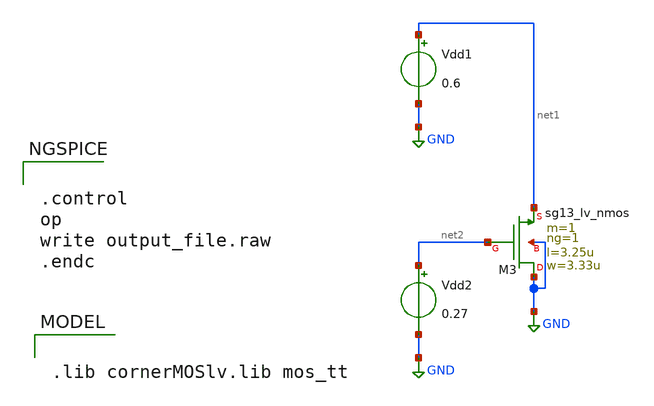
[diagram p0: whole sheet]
** sch_path: modules/module_0_foundations/xschem/nmos_gmid.sch
**.subckt nmos_gmid
XM3 GND net2 net1 GND sg13_lv_nmos w=3.33u l=3.25u ng=1 m=1 mm_ok=1
Vdd1 net1 GND 0.6
Vdd2 net2 GND 0.27
**** begin user architecture code

.lib cornerMOSlv.lib mos_tt



.control
op
write output_file.raw
.endc


**** end user architecture code
**.ends
.GLOBAL GND
.end
